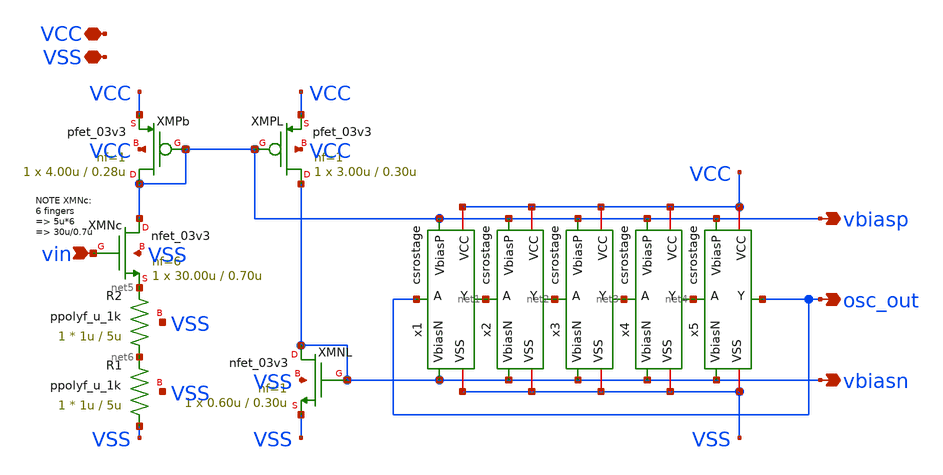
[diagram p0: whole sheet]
** sch_path: xschem/csringosc.sch
**.subckt csringosc osc_out vin VCC VSS vbiasp vbiasn
*.opin osc_out
*.ipin vin
*.iopin VCC
*.iopin VSS
*.opin vbiasp
*.opin vbiasn
x1 VCC VSS vbiasp osc_out net1 vbiasn csrostage
x2 VCC VSS vbiasp net1 net2 vbiasn csrostage
x3 VCC VSS vbiasp net2 net3 vbiasn csrostage
x4 VCC VSS vbiasp net3 net4 vbiasn csrostage
x5 VCC VSS vbiasp net4 osc_out vbiasn csrostage
XMNL vbiasn vbiasn VSS VSS nfet_03v3 L=0.30u W=0.60u nf=1 ad='int((nf+1)/2) * W/nf * 0.18u' as='int((nf+2)/2) * W/nf * 0.18u'
+ pd='2*int((nf+1)/2) * (W/nf + 0.18u)' ps='2*int((nf+2)/2) * (W/nf + 0.18u)' nrd='0.18u / W' nrs='0.18u / W'
+ sa=0 sb=0 sd=0 m=1
XMPL vbiasn vbiasp VCC VCC pfet_03v3 L=0.30u W=3.00u nf=1 ad='int((nf+1)/2) * W/nf * 0.18u' as='int((nf+2)/2) * W/nf * 0.18u'
+ pd='2*int((nf+1)/2) * (W/nf + 0.18u)' ps='2*int((nf+2)/2) * (W/nf + 0.18u)' nrd='0.18u / W' nrs='0.18u / W'
+ sa=0 sb=0 sd=0 m=1
XMPb vbiasp vbiasp VCC VCC pfet_03v3 L=0.28u W=4.00u nf=1 ad='int((nf+1)/2) * W/nf * 0.18u' as='int((nf+2)/2) * W/nf * 0.18u'
+ pd='2*int((nf+1)/2) * (W/nf + 0.18u)' ps='2*int((nf+2)/2) * (W/nf + 0.18u)' nrd='0.18u / W' nrs='0.18u / W'
+ sa=0 sb=0 sd=0 m=1
XMNc vbiasp vin net5 VSS nfet_03v3 L=0.70u W=30.00u nf=6 ad='int((nf+1)/2) * W/nf * 0.18u' as='int((nf+2)/2) * W/nf * 0.18u'
+ pd='2*int((nf+1)/2) * (W/nf + 0.18u)' ps='2*int((nf+2)/2) * (W/nf + 0.18u)' nrd='0.18u / W' nrs='0.18u / W'
+ sa=0 sb=0 sd=0 m=1
XR2 net6 net5 VSS ppolyf_u_1k r_width=1u r_length=5u m=1
XR1 VSS net6 VSS ppolyf_u_1k r_width=1u r_length=5u m=1
**.ends

* expanding   symbol:  csrostage.sym # of pins=6
** sym_path: xschem/csrostage.sym
** sch_path: xschem/csrostage.sch
.subckt csrostage VCC VSS VbiasP A Y VbiasN
*.iopin VCC
*.iopin VSS
*.ipin A
*.opin Y
*.ipin VbiasP
*.ipin VbiasN
XM1 Y A net1 VSS nfet_03v3 L=0.50u W=0.25u nf=1 ad='int((nf+1)/2) * W/nf * 0.18u' as='int((nf+2)/2) * W/nf * 0.18u'
+ pd='2*int((nf+1)/2) * (W/nf + 0.18u)' ps='2*int((nf+2)/2) * (W/nf + 0.18u)' nrd='0.18u / W' nrs='0.18u / W'
+ sa=0 sb=0 sd=0 m=1
XM2 Y A net2 VCC pfet_03v3 L=0.50u W=0.50u nf=1 ad='int((nf+1)/2) * W/nf * 0.18u' as='int((nf+2)/2) * W/nf * 0.18u'
+ pd='2*int((nf+1)/2) * (W/nf + 0.18u)' ps='2*int((nf+2)/2) * (W/nf + 0.18u)' nrd='0.18u / W' nrs='0.18u / W'
+ sa=0 sb=0 sd=0 m=1
XM3 net2 VbiasP VCC VCC pfet_03v3 L=0.50u W=0.50u nf=1 ad='int((nf+1)/2) * W/nf * 0.18u' as='int((nf+2)/2) * W/nf * 0.18u'
+ pd='2*int((nf+1)/2) * (W/nf + 0.18u)' ps='2*int((nf+2)/2) * (W/nf + 0.18u)' nrd='0.18u / W' nrs='0.18u / W'
+ sa=0 sb=0 sd=0 m=1
XM4 net1 VbiasN VSS VSS nfet_03v3 L=0.50u W=0.25u nf=1 ad='int((nf+1)/2) * W/nf * 0.18u' as='int((nf+2)/2) * W/nf * 0.18u'
+ pd='2*int((nf+1)/2) * (W/nf + 0.18u)' ps='2*int((nf+2)/2) * (W/nf + 0.18u)' nrd='0.18u / W' nrs='0.18u / W'
+ sa=0 sb=0 sd=0 m=1
.ends

.end
